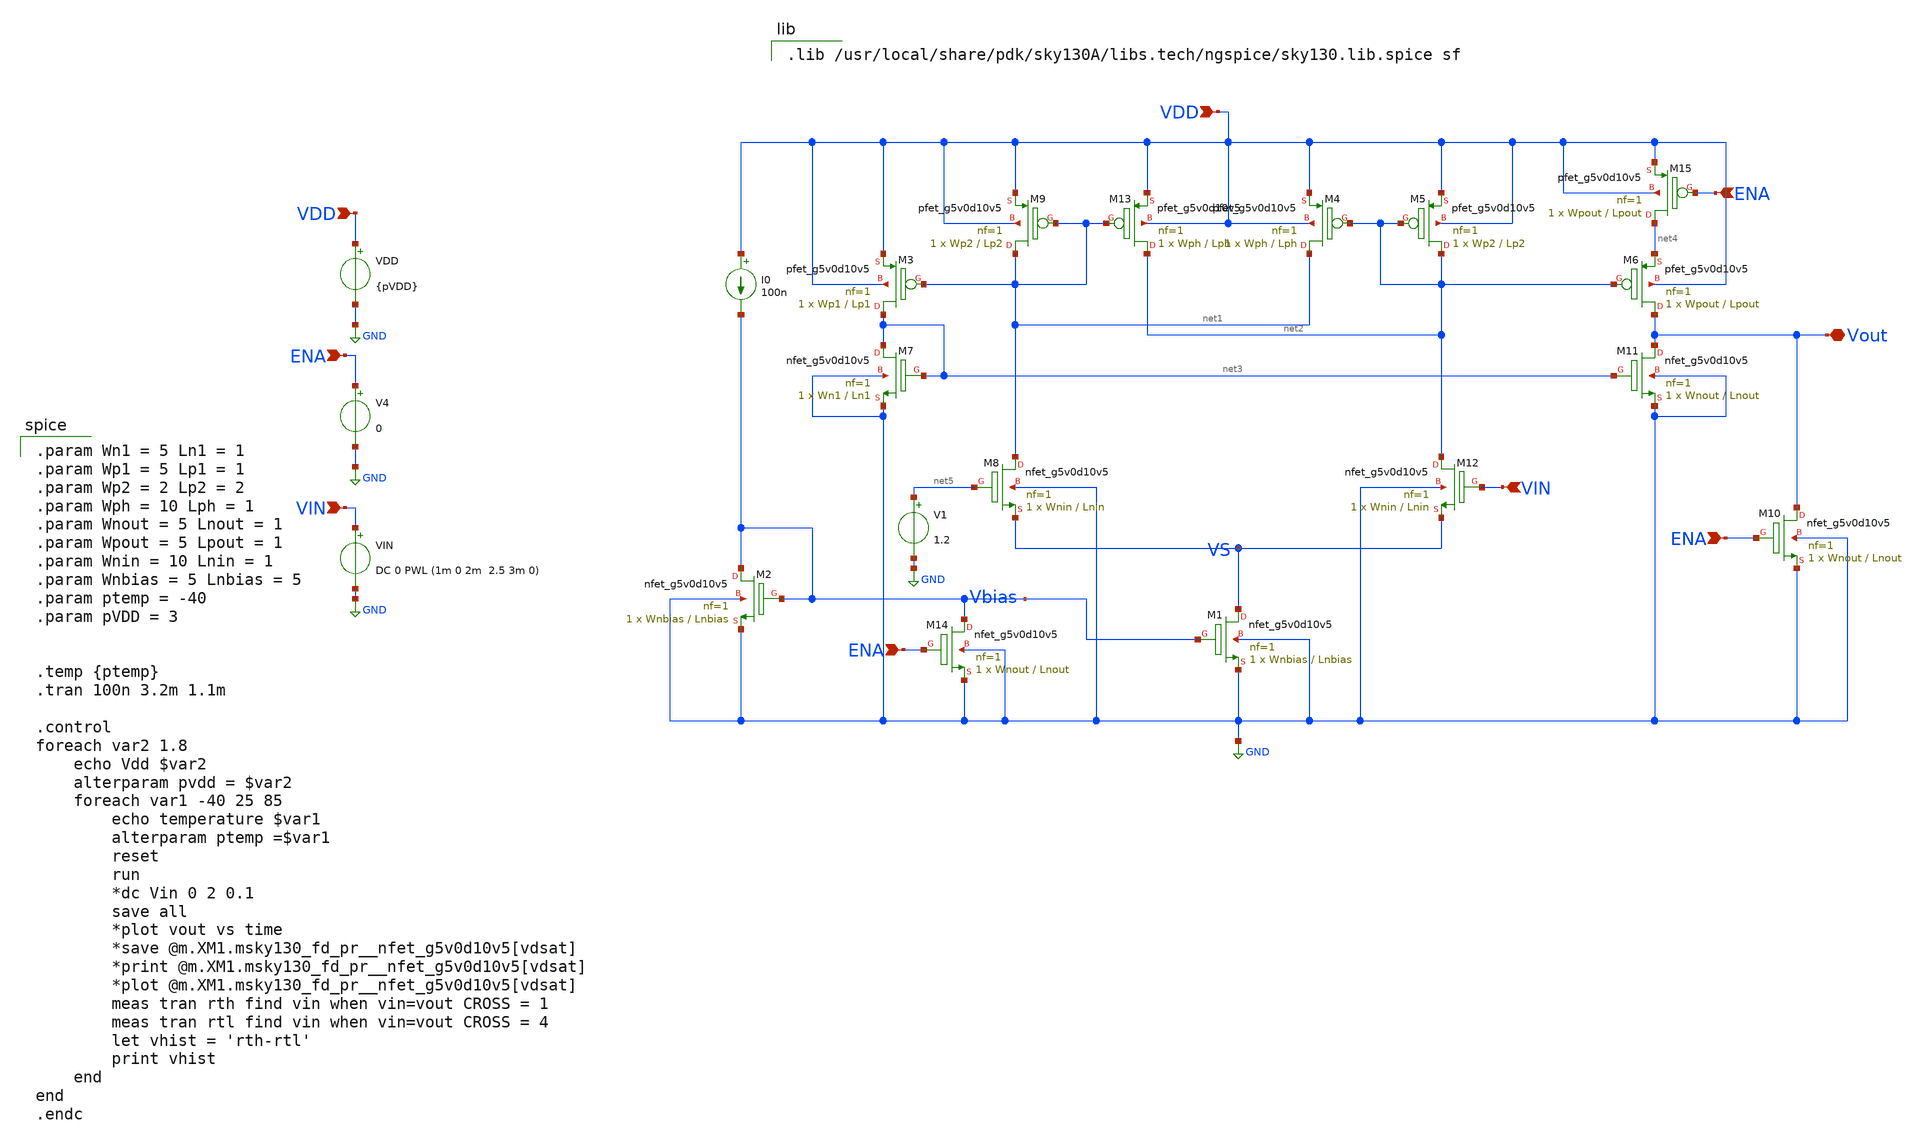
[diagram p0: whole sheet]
** sch_path: xschem/Comparador_Digital_Voltage_Final.sch
**.subckt Comparador_Digital_Voltage_Final VDD VDD Vout VIN VIN ENA ENA ENA ENA
*.ipin VDD
*.ipin VDD
*.iopin Vout
*.ipin VIN
*.ipin VIN
*.ipin ENA
*.ipin ENA
*.ipin ENA
*.ipin ENA
V1 net5 GND 1.2
VDD VDD GND {pVDD}
VIN VIN GND DC 0 PWL (1m 0 2m 2.5 3m 0)
I0 VDD Vbias 100n
XM3 net3 net1 VDD VDD sky130_fd_pr__pfet_g5v0d10v5 L=Lp1 W=Wp1 nf=1 ad='int((nf+1)/2) * W/nf * 0.29'
+ as='int((nf+2)/2) * W/nf * 0.29' pd='2*int((nf+1)/2) * (W/nf + 0.29)' ps='2*int((nf+2)/2) * (W/nf + 0.29)'
+ nrd='0.29 / W' nrs='0.29 / W' sa=0 sb=0 sd=0 mult=1 m=1
XM9 net1 net1 VDD VDD sky130_fd_pr__pfet_g5v0d10v5 L=Lp2 W=Wp2 nf=1 ad='int((nf+1)/2) * W/nf * 0.29'
+ as='int((nf+2)/2) * W/nf * 0.29' pd='2*int((nf+1)/2) * (W/nf + 0.29)' ps='2*int((nf+2)/2) * (W/nf + 0.29)'
+ nrd='0.29 / W' nrs='0.29 / W' sa=0 sb=0 sd=0 mult=1 m=1
XM13 net2 net1 VDD VDD sky130_fd_pr__pfet_g5v0d10v5 L=Lph W=Wph nf=1 ad='int((nf+1)/2) * W/nf * 0.29'
+ as='int((nf+2)/2) * W/nf * 0.29' pd='2*int((nf+1)/2) * (W/nf + 0.29)' ps='2*int((nf+2)/2) * (W/nf + 0.29)'
+ nrd='0.29 / W' nrs='0.29 / W' sa=0 sb=0 sd=0 mult=1 m=1
XM4 net1 net2 VDD VDD sky130_fd_pr__pfet_g5v0d10v5 L=Lph W=Wph nf=1 ad='int((nf+1)/2) * W/nf * 0.29'
+ as='int((nf+2)/2) * W/nf * 0.29' pd='2*int((nf+1)/2) * (W/nf + 0.29)' ps='2*int((nf+2)/2) * (W/nf + 0.29)'
+ nrd='0.29 / W' nrs='0.29 / W' sa=0 sb=0 sd=0 mult=1 m=1
XM5 net2 net2 VDD VDD sky130_fd_pr__pfet_g5v0d10v5 L=Lp2 W=Wp2 nf=1 ad='int((nf+1)/2) * W/nf * 0.29'
+ as='int((nf+2)/2) * W/nf * 0.29' pd='2*int((nf+1)/2) * (W/nf + 0.29)' ps='2*int((nf+2)/2) * (W/nf + 0.29)'
+ nrd='0.29 / W' nrs='0.29 / W' sa=0 sb=0 sd=0 mult=1 m=1
XM6 Vout net2 net4 VDD sky130_fd_pr__pfet_g5v0d10v5 L=Lpout W=Wpout nf=1 ad='int((nf+1)/2) * W/nf * 0.29'
+ as='int((nf+2)/2) * W/nf * 0.29' pd='2*int((nf+1)/2) * (W/nf + 0.29)' ps='2*int((nf+2)/2) * (W/nf + 0.29)'
+ nrd='0.29 / W' nrs='0.29 / W' sa=0 sb=0 sd=0 mult=1 m=1
XM11 Vout net3 GND GND sky130_fd_pr__nfet_g5v0d10v5 L=Lnout W=Wnout nf=1 ad='int((nf+1)/2) * W/nf * 0.29'
+ as='int((nf+2)/2) * W/nf * 0.29' pd='2*int((nf+1)/2) * (W/nf + 0.29)' ps='2*int((nf+2)/2) * (W/nf + 0.29)'
+ nrd='0.29 / W' nrs='0.29 / W' sa=0 sb=0 sd=0 mult=1 m=1
XM7 net3 net3 GND GND sky130_fd_pr__nfet_g5v0d10v5 L=Ln1 W=Wn1 nf=1 ad='int((nf+1)/2) * W/nf * 0.29'
+ as='int((nf+2)/2) * W/nf * 0.29' pd='2*int((nf+1)/2) * (W/nf + 0.29)' ps='2*int((nf+2)/2) * (W/nf + 0.29)'
+ nrd='0.29 / W' nrs='0.29 / W' sa=0 sb=0 sd=0 mult=1 m=1
XM10 Vout ENA GND GND sky130_fd_pr__nfet_g5v0d10v5 L=Lnout W=Wnout nf=1 ad='int((nf+1)/2) * W/nf * 0.29'
+ as='int((nf+2)/2) * W/nf * 0.29' pd='2*int((nf+1)/2) * (W/nf + 0.29)' ps='2*int((nf+2)/2) * (W/nf + 0.29)'
+ nrd='0.29 / W' nrs='0.29 / W' sa=0 sb=0 sd=0 mult=1 m=1
XM14 Vbias ENA GND GND sky130_fd_pr__nfet_g5v0d10v5 L=Lnout W=Wnout nf=1 ad='int((nf+1)/2) * W/nf * 0.29'
+ as='int((nf+2)/2) * W/nf * 0.29' pd='2*int((nf+1)/2) * (W/nf + 0.29)' ps='2*int((nf+2)/2) * (W/nf + 0.29)'
+ nrd='0.29 / W' nrs='0.29 / W' sa=0 sb=0 sd=0 mult=1 m=1
V4 ENA GND 0
XM15 net4 ENA VDD VDD sky130_fd_pr__pfet_g5v0d10v5 L=Lpout W=Wpout nf=1 ad='int((nf+1)/2) * W/nf * 0.29'
+ as='int((nf+2)/2) * W/nf * 0.29' pd='2*int((nf+1)/2) * (W/nf + 0.29)' ps='2*int((nf+2)/2) * (W/nf + 0.29)'
+ nrd='0.29 / W' nrs='0.29 / W' sa=0 sb=0 sd=0 mult=1 m=1
XM8 net1 net5 VS GND sky130_fd_pr__nfet_g5v0d10v5 L=Lnin W=Wnin nf=1 ad='int((nf+1)/2) * W/nf * 0.29'
+ as='int((nf+2)/2) * W/nf * 0.29' pd='2*int((nf+1)/2) * (W/nf + 0.29)' ps='2*int((nf+2)/2) * (W/nf + 0.29)'
+ nrd='0.29 / W' nrs='0.29 / W' sa=0 sb=0 sd=0 mult=1 m=1
XM12 net2 VIN VS GND sky130_fd_pr__nfet_g5v0d10v5 L=Lnin W=Wnin nf=1 ad='int((nf+1)/2) * W/nf * 0.29'
+ as='int((nf+2)/2) * W/nf * 0.29' pd='2*int((nf+1)/2) * (W/nf + 0.29)' ps='2*int((nf+2)/2) * (W/nf + 0.29)'
+ nrd='0.29 / W' nrs='0.29 / W' sa=0 sb=0 sd=0 mult=1 m=1
XM1 VS Vbias GND GND sky130_fd_pr__nfet_g5v0d10v5 L=Lnbias W=Wnbias nf=1 ad='int((nf+1)/2) * W/nf * 0.29'
+ as='int((nf+2)/2) * W/nf * 0.29' pd='2*int((nf+1)/2) * (W/nf + 0.29)' ps='2*int((nf+2)/2) * (W/nf + 0.29)'
+ nrd='0.29 / W' nrs='0.29 / W' sa=0 sb=0 sd=0 mult=1 m=1
XM2 Vbias Vbias GND GND sky130_fd_pr__nfet_g5v0d10v5 L=Lnbias W=Wnbias nf=1 ad='int((nf+1)/2) * W/nf * 0.29'
+ as='int((nf+2)/2) * W/nf * 0.29' pd='2*int((nf+1)/2) * (W/nf + 0.29)' ps='2*int((nf+2)/2) * (W/nf + 0.29)'
+ nrd='0.29 / W' nrs='0.29 / W' sa=0 sb=0 sd=0 mult=1 m=1
**** begin user architecture code

.param Wn1 = 5 Ln1 = 1
.param Wp1 = 5 Lp1 = 1
.param Wp2 = 2 Lp2 = 2
.param Wph = 10 Lph = 1
.param Wnout = 5 Lnout = 1
.param Wpout = 5 Lpout = 1
.param Wnin = 10 Lnin = 1
.param Wnbias = 5 Lnbias = 5
.param ptemp = -40
.param pVDD = 3


.temp {ptemp}
.tran 100n 3.2m 1.1m

.control
foreach var2 1.8
	echo Vdd $var2
	alterparam pvdd = $var2
	foreach var1 -40 25 85
		echo temperature $var1
		alterparam ptemp =$var1
		reset
		run
		*dc Vin 0 2 0.1
		save all
		*plot vout vs time
		*save @m.XM1.msky130_fd_pr__nfet_g5v0d10v5[vdsat]
		*print @m.XM1.msky130_fd_pr__nfet_g5v0d10v5[vdsat]
		*plot @m.XM1.msky130_fd_pr__nfet_g5v0d10v5[vdsat]
		meas tran rth find vin when vin=vout CROSS = 1
		meas tran rtl find vin when vin=vout CROSS = 4
		let vhist = 'rth-rtl'
		print vhist
	end
end
.endc


.lib /usr/local/share/pdk/sky130A/libs.tech/ngspice/sky130.lib.spice sf

**** end user architecture code
**.ends
.GLOBAL GND
.end
